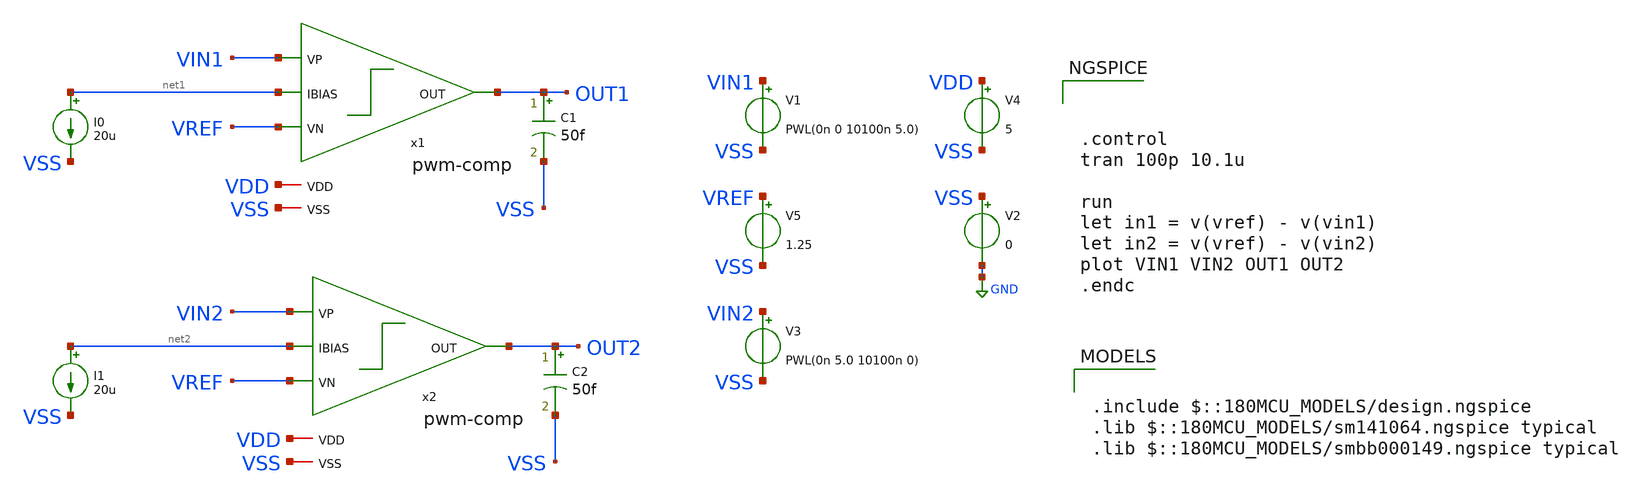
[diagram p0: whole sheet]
** sch_path: designs/pwm-comparator/pwm-comp-tb.sch
**.subckt pwm-comp-tb
x1 VDD net1 OUT1 VIN1 VREF VSS pwm-comp
x2 VDD net2 OUT2 VIN2 VREF VSS pwm-comp
I0 net1 VSS 20u
I1 net2 VSS 20u
C1 OUT1 VSS 50f m=1
C2 OUT2 VSS 50f m=1
V1 VIN1 VSS PWL(0n 0 10100n 5.0)
V3 VIN2 VSS PWL(0n 5.0 10100n 0)
V4 VDD VSS 5
V5 VREF VSS 1.25
V2 VSS GND 0
**** begin user architecture code



.control
tran 100p 10.1u

run
let in1 = v(vref) - v(vin1)
let in2 = v(vref) - v(vin2)
plot VIN1 VIN2 OUT1 OUT2
.endc



.include $::180MCU_MODELS/design.ngspice
.lib $::180MCU_MODELS/sm141064.ngspice typical
.lib $::180MCU_MODELS/smbb000149.ngspice typical

**** end user architecture code
**.ends

* expanding   symbol:  pwm-comp.sym # of pins=6
** sym_path: designs/pwm-comparator/pwm-comp.sym
** sch_path: designs/pwm-comparator/pwm-comp.sch
.subckt pwm-comp VDD IBIAS OUT VP VN VSS
*.ipin VN
*.ipin VP
*.opin OUT
*.iopin VDD
*.iopin VSS
*.ipin IBIAS
XM3 net2 VP net3 VDD pfet_05v0 L=1u W=51u nf=1 ad='int((nf+1)/2) * W/nf * 0.18u' as='int((nf+2)/2) * W/nf * 0.18u'
+ pd='2*int((nf+1)/2) * (W/nf + 0.18u)' ps='2*int((nf+2)/2) * (W/nf + 0.18u)' nrd='0.18u / W' nrs='0.18u / W'
+ sa=0 sb=0 sd=0 m=1
XM4 net1 VN net3 VDD pfet_05v0 L=1u W=51u nf=1 ad='int((nf+1)/2) * W/nf * 0.18u' as='int((nf+2)/2) * W/nf * 0.18u'
+ pd='2*int((nf+1)/2) * (W/nf + 0.18u)' ps='2*int((nf+2)/2) * (W/nf + 0.18u)' nrd='0.18u / W' nrs='0.18u / W'
+ sa=0 sb=0 sd=0 m=1
XM5 net2 net1 VSS VSS nfet_05v0 L=1u W=20u nf=1 ad='int((nf+1)/2) * W/nf * 0.18u' as='int((nf+2)/2) * W/nf * 0.18u'
+ pd='2*int((nf+1)/2) * (W/nf + 0.18u)' ps='2*int((nf+2)/2) * (W/nf + 0.18u)' nrd='0.18u / W' nrs='0.18u / W'
+ sa=0 sb=0 sd=0 m=1
XM6 net1 net1 VSS VSS nfet_05v0 L=1u W=20u nf=1 ad='int((nf+1)/2) * W/nf * 0.18u' as='int((nf+2)/2) * W/nf * 0.18u'
+ pd='2*int((nf+1)/2) * (W/nf + 0.18u)' ps='2*int((nf+2)/2) * (W/nf + 0.18u)' nrd='0.18u / W' nrs='0.18u / W'
+ sa=0 sb=0 sd=0 m=1
XM7 OUT net2 VSS VSS nfet_05v0 L=0.75u W=8.5u nf=1 ad='int((nf+1)/2) * W/nf * 0.18u' as='int((nf+2)/2) * W/nf * 0.18u'
+ pd='2*int((nf+1)/2) * (W/nf + 0.18u)' ps='2*int((nf+2)/2) * (W/nf + 0.18u)' nrd='0.18u / W' nrs='0.18u / W'
+ sa=0 sb=0 sd=0 m=1
XM8 OUT IBIAS VDD VDD pfet_05v0 L=0.75u W=40u nf=1 ad='int((nf+1)/2) * W/nf * 0.18u' as='int((nf+2)/2) * W/nf * 0.18u'
+ pd='2*int((nf+1)/2) * (W/nf + 0.18u)' ps='2*int((nf+2)/2) * (W/nf + 0.18u)' nrd='0.18u / W' nrs='0.18u / W'
+ sa=0 sb=0 sd=0 m=1
XM1 net3 IBIAS VDD VDD pfet_05v0 L=1u W=79u nf=1 ad='int((nf+1)/2) * W/nf * 0.18u' as='int((nf+2)/2) * W/nf * 0.18u'
+ pd='2*int((nf+1)/2) * (W/nf + 0.18u)' ps='2*int((nf+2)/2) * (W/nf + 0.18u)' nrd='0.18u / W' nrs='0.18u / W'
+ sa=0 sb=0 sd=0 m=1
XM2 IBIAS IBIAS VDD VDD pfet_05v0 L=1u W=79u nf=1 ad='int((nf+1)/2) * W/nf * 0.18u' as='int((nf+2)/2) * W/nf * 0.18u'
+ pd='2*int((nf+1)/2) * (W/nf + 0.18u)' ps='2*int((nf+2)/2) * (W/nf + 0.18u)' nrd='0.18u / W' nrs='0.18u / W'
+ sa=0 sb=0 sd=0 m=1
.ends

.GLOBAL GND
.end
